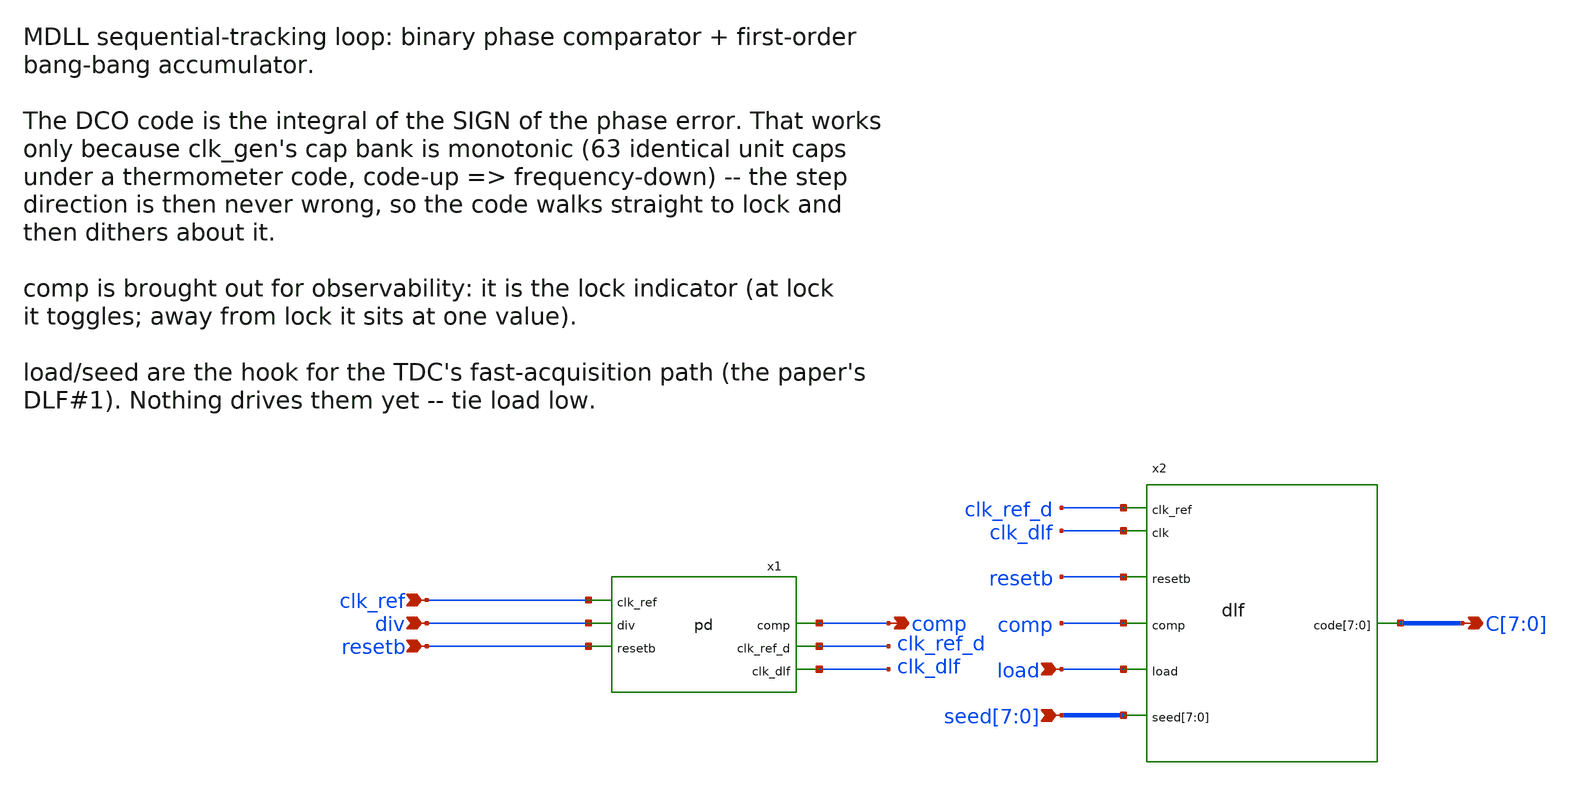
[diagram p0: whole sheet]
** sch_path: TPU5555-main/mdll/mixed_signal_design_blocks/bbpd/src/bbpd.sch
* IHP-GmbH/IHP-Open-PDK/ihp-sg13g2/libs.tech/xschem/sg13g2_stdcells/sg13g2_buf_4.sch:
* Copyright 2023 IHP PDK Authors
* Licensed under the Apache License, Version 2.0 (the "License");
**.subckt bbpd clk_ref div resetb load
*+ seed[7],seed[6],seed[5],seed[4],seed[3],seed[2],seed[1],seed[0] C[7],C[6],C[5],C[4],C[3],C[2],C[1],C[0] comp
*.ipin clk_ref
*.ipin div
*.ipin resetb
*.ipin load
*.ipin seed[7],seed[6],seed[5],seed[4],seed[3],seed[2],seed[1],seed[0]
*.opin C[7],C[6],C[5],C[4],C[3],C[2],C[1],C[0]
*.opin comp
x1 clk_ref div resetb comp clk_ref_d clk_dlf pd
x2 clk_ref_d clk_dlf resetb comp load seed[7] seed[6] seed[5] seed[4] seed[3] seed[2] seed[1]
+ seed[0] C[7] C[6] C[5] C[4] C[3] C[2] C[1] C[0] dlf
**.ends

* expanding   symbol:  bbpd/src/pd.sym # of pins=6
** sym_path: TPU5555-main/mdll/mixed_signal_design_blocks/bbpd/src/pd.sym
** sch_path: TPU5555-main/mdll/mixed_signal_design_blocks/bbpd/src/pd.sch
.subckt pd clk_ref div resetb comp clk_ref_d clk_dlf
*.ipin div
*.ipin clk_ref
*.ipin resetb
*.opin comp
*.opin clk_ref_d
*.opin clk_dlf
x1 comp_raw div clk_ref resetb VDD VSS sg13g2_dfrbpq_1
x2 comp clk_x2 comp_raw resetb VDD VSS sg13g2_dfrbpq_2
x7 clk_x2 clk_ref_d VDD VSS sg13g2_dlygate4sd3_1
x6 clk_ref_d clk_ref VDD VSS sg13g2_buf_2
x8 net1 clk_x2 VDD VSS sg13g2_dlygate4sd3_1
x9 net2 net1 VDD VSS sg13g2_dlygate4sd3_1
x10 clk_dlf net2 VDD VSS sg13g2_buf_4
.ends


* expanding   symbol:  sg13g2_dfrbpq_1.sym # of pins=4
** sym_path: sg13g2_dfrbpq_1.sym
** sch_path: sg13g2_dfrbpq_1.sch
.subckt sg13g2_dfrbpq_1 Q CLK D RESET_B VDD VSS
*.opin Q
*.ipin CLK
*.ipin D
*.ipin RESET_B
*.iopin VDD
*.iopin VSS
XM1 Db D net10 VSS sg13_lv_nmos w=420.00n l=130.00n ng=1 m=1 mm_ok=1
XM2 net10 RESET_B VSS VSS sg13_lv_nmos w=420.00n l=130.00n ng=1 m=1 mm_ok=1
XM3 net1 clkneg net9 VSS sg13_lv_nmos w=420.00n l=130.00n ng=1 m=1 mm_ok=1
XM4 net9 net1 VSS VSS sg13_lv_nmos w=420.00n l=130.00n ng=1 m=1 mm_ok=1
XM5 net1 net1 net5 VSS sg13_lv_nmos w=420.00n l=130.00n ng=1 m=1 mm_ok=1
XM6 net5 RESET_B VSS VSS sg13_lv_nmos w=420.00n l=130.00n ng=1 m=1 mm_ok=1
XM7 net2 net1 VSS VSS sg13_lv_nmos w=740.00n l=130.00n ng=1 m=1 mm_ok=1
XM8 Q net2 VSS VSS sg13_lv_nmos w=740.00n l=130.00n ng=1 m=1 mm_ok=1
XM9 clkneg CLK VSS VSS sg13_lv_nmos w=740.00n l=130.00n ng=1 m=1 mm_ok=1
XM10 clkpos clkneg VSS VSS sg13_lv_nmos w=740.00n l=130.00n ng=1 m=1 mm_ok=1
XM11 Db clkneg net3 VSS sg13_lv_nmos w=420.00n l=130.00n ng=1 m=1 mm_ok=1
XM12 net3 clkpos net8 VSS sg13_lv_nmos w=420.00n l=130.00n ng=1 m=1 mm_ok=1
XM13 net8 net3 net4 VSS sg13_lv_nmos w=420.00n l=130.00n ng=1 m=1 mm_ok=1
XM14 net4 RESET_B VSS VSS sg13_lv_nmos w=420.00n l=130.00n ng=1 m=1 mm_ok=1
XM15 net3 net3 VSS VSS sg13_lv_nmos w=740.00n l=130.00n ng=1 m=1 mm_ok=1
XM16 net3 clkpos net1 VSS sg13_lv_nmos w=740.00n l=130.00n ng=1 m=1 mm_ok=1
XM17 Db RESET_B VDD VDD sg13_lv_pmos w=420.00n l=130.00n ng=1 m=1 mm_ok=1
XM18 Db D VDD VDD sg13_lv_pmos w=420.00n l=130.00n ng=1 m=1 mm_ok=1
XM19 net7 net1 VDD VDD sg13_lv_pmos w=420.00n l=130.00n ng=1 m=1 mm_ok=1
XM20 net1 clkpos net7 VDD sg13_lv_pmos w=420.00n l=130.00n ng=1 m=1 mm_ok=1
XM21 net1 net1 VDD VDD sg13_lv_pmos w=420.00n l=130.00n ng=1 m=1 mm_ok=1
XM22 net1 RESET_B VDD VDD sg13_lv_pmos w=420.00n l=130.00n ng=1 m=1 mm_ok=1
XM23 net2 net1 VDD VDD sg13_lv_pmos w=1.12u l=130.00n ng=1 m=1 mm_ok=1
XM24 Q net2 VDD VDD sg13_lv_pmos w=1.12u l=130.00n ng=1 m=1 mm_ok=1
XM25 clkneg CLK VDD VDD sg13_lv_pmos w=1.12u l=130.00n ng=1 m=1 mm_ok=1
XM26 clkpos clkneg VDD VDD sg13_lv_pmos w=1.12u l=130.00n ng=1 m=1 mm_ok=1
XM27 Db clkpos net3 VDD sg13_lv_pmos w=420.00n l=130.00n ng=1 m=1 mm_ok=1
XM28 net6 net3 VDD VDD sg13_lv_pmos w=420.00n l=130.00n ng=1 m=1 mm_ok=1
XM29 net3 clkneg net6 VDD sg13_lv_pmos w=420.00n l=130.00n ng=1 m=1 mm_ok=1
XM30 net3 RESET_B VDD VDD sg13_lv_pmos w=420.00n l=130.00n ng=1 m=1 mm_ok=1
XM31 net3 net3 VDD VDD sg13_lv_pmos w=1.000u l=130.00n ng=1 m=1 mm_ok=1
XM32 net3 clkneg net1 VDD sg13_lv_pmos w=1.000u l=130.00n ng=1 m=1 mm_ok=1
.ends


* expanding   symbol:  sg13g2_dfrbpq_2.sym # of pins=4
** sym_path: sg13g2_dfrbpq_2.sym
** sch_path: sg13g2_dfrbpq_2.sch
.subckt sg13g2_dfrbpq_2 Q CLK D RESET_B VDD VSS
*.opin Q
*.ipin CLK
*.ipin D
*.ipin RESET_B
*.iopin VDD
*.iopin VSS
XM1 Db D net12 VSS sg13_lv_nmos w=420.00n l=130.00n ng=1 m=1 mm_ok=1
XM2 net12 RESET_B VSS VSS sg13_lv_nmos w=420.00n l=130.00n ng=1 m=1 mm_ok=1
XM3 net2 clkneg net11 VSS sg13_lv_nmos w=420.00n l=130.00n ng=1 m=1 mm_ok=1
XM4 net11 net3 VSS VSS sg13_lv_nmos w=420.00n l=130.00n ng=1 m=1 mm_ok=1
XM5 net3 net2 net7 VSS sg13_lv_nmos w=420.00n l=130.00n ng=1 m=1 mm_ok=1
XM6 net7 RESET_B VSS VSS sg13_lv_nmos w=420.00n l=130.00n ng=1 m=1 mm_ok=1
XM7 net1 net2 VSS VSS sg13_lv_nmos w=640.00n l=130.00n ng=1 m=1 mm_ok=1
XM8 Q net1 VSS VSS sg13_lv_nmos w=1.48u l=130.00n ng=2 m=1 mm_ok=1
XM9 clkneg CLK VSS VSS sg13_lv_nmos w=740.00n l=130.00n ng=1 m=1 mm_ok=1
XM10 clkpos clkneg VSS VSS sg13_lv_nmos w=740.00n l=130.00n ng=1 m=1 mm_ok=1
XM11 Db clkneg net4 VSS sg13_lv_nmos w=420.00n l=130.00n ng=1 m=1 mm_ok=1
XM12 net4 clkpos net10 VSS sg13_lv_nmos w=420.00n l=130.00n ng=1 m=1 mm_ok=1
XM13 net10 net5 net6 VSS sg13_lv_nmos w=420.00n l=130.00n ng=1 m=1 mm_ok=1
XM14 net6 RESET_B VSS VSS sg13_lv_nmos w=420.00n l=130.00n ng=1 m=1 mm_ok=1
XM15 net5 net4 VSS VSS sg13_lv_nmos w=740.00n l=130.00n ng=1 m=1 mm_ok=1
XM16 net5 clkpos net2 VSS sg13_lv_nmos w=740.00n l=130.00n ng=1 m=1 mm_ok=1
XM17 Db RESET_B VDD VDD sg13_lv_pmos w=420.00n l=130.00n ng=1 m=1 mm_ok=1
XM18 Db D VDD VDD sg13_lv_pmos w=420.00n l=130.00n ng=1 m=1 mm_ok=1
XM19 net9 net3 VDD VDD sg13_lv_pmos w=420.00n l=130.00n ng=1 m=1 mm_ok=1
XM20 net2 clkpos net9 VDD sg13_lv_pmos w=420.00n l=130.00n ng=1 m=1 mm_ok=1
XM21 net3 net2 VDD VDD sg13_lv_pmos w=420.00n l=130.00n ng=1 m=1 mm_ok=1
XM22 net3 RESET_B VDD VDD sg13_lv_pmos w=420.00n l=130.00n ng=1 m=1 mm_ok=1
XM23 net1 net2 VDD VDD sg13_lv_pmos w=1.000u l=130.00n ng=1 m=1 mm_ok=1
XM24 Q net1 VDD VDD sg13_lv_pmos w=2.24u l=130.00n ng=2 m=1 mm_ok=1
XM25 clkneg CLK VDD VDD sg13_lv_pmos w=1.12u l=130.00n ng=1 m=1 mm_ok=1
XM26 clkpos clkneg VDD VDD sg13_lv_pmos w=1.12u l=130.00n ng=1 m=1 mm_ok=1
XM27 Db clkpos net4 VDD sg13_lv_pmos w=420.00n l=130.00n ng=1 m=1 mm_ok=1
XM28 net8 net5 VDD VDD sg13_lv_pmos w=420.00n l=130.00n ng=1 m=1 mm_ok=1
XM29 net4 clkneg net8 VDD sg13_lv_pmos w=420.00n l=130.00n ng=1 m=1 mm_ok=1
XM30 net4 RESET_B VDD VDD sg13_lv_pmos w=420.00n l=130.00n ng=1 m=1 mm_ok=1
XM31 net5 net4 VDD VDD sg13_lv_pmos w=1.000u l=130.00n ng=1 m=1 mm_ok=1
XM32 net5 clkneg net2 VDD sg13_lv_pmos w=1.000u l=130.00n ng=1 m=1 mm_ok=1
.ends


* expanding   symbol:  sg13g2_dlygate4sd3_1.sym # of pins=2
** sym_path: sg13g2_dlygate4sd3_1.sym
** sch_path: sg13g2_dlygate4sd3_1.sch
.subckt sg13g2_dlygate4sd3_1 X A VDD VSS
*.ipin A
*.opin X
*.iopin VDD
*.iopin VSS
XM1 net3 A VSS VSS sg13_lv_nmos w=420.00n l=130.00n ng=1 m=1 mm_ok=1
XM2 net1 net3 VSS VSS sg13_lv_nmos w=420.00n l=500.0n ng=1 m=1 mm_ok=1
XM3 net2 net1 VSS VSS sg13_lv_nmos w=420.00n l=500.0n ng=1 m=1 mm_ok=1
XM4 X net2 VSS VSS sg13_lv_nmos w=740.00n l=130.00n ng=1 m=1 mm_ok=1
XM5 net3 A VDD VDD sg13_lv_pmos w=420.00n l=130.00n ng=1 m=1 mm_ok=1
XM6 net1 net3 VDD VDD sg13_lv_pmos w=1.000u l=500.0n ng=1 m=1 mm_ok=1
XM7 net2 net1 VDD VDD sg13_lv_pmos w=1.000u l=500.0n ng=1 m=1 mm_ok=1
XM8 X net2 VDD VDD sg13_lv_pmos w=1.12u l=130.00n ng=1 m=1 mm_ok=1
.ends


* expanding   symbol:  sg13g2_buf_2.sym # of pins=2
** sym_path: sg13g2_buf_2.sym
** sch_path: sg13g2_buf_2.sch
.subckt sg13g2_buf_2 X A VDD VSS
*.ipin A
*.opin X
*.iopin VDD
*.iopin VSS
XM1 net1 A VSS VSS sg13_lv_nmos w=640.00n l=130.00n ng=1 m=1 mm_ok=1
XM2 X net1 VSS VSS sg13_lv_nmos w=1.48u l=130.00n ng=2 m=1 mm_ok=1
XM3 net1 A VDD VDD sg13_lv_pmos w=1.000u l=130.00n ng=1 m=1 mm_ok=1
XM4 X net1 VDD VDD sg13_lv_pmos w=2.24u l=130.00n ng=2 m=1 mm_ok=1
.ends


* expanding   symbol:  sg13g2_buf_4.sym # of pins=2
** sym_path: sg13g2_buf_4.sym
** sch_path: sg13g2_buf_4.sch
.subckt sg13g2_buf_4 X A VDD VSS
*.ipin A
*.opin X
*.iopin VDD
*.iopin VSS
XM1 net1 A VSS VSS sg13_lv_nmos w=740.00n l=130.00n ng=1 m=1 mm_ok=1
XM2 X net1 VSS VSS sg13_lv_nmos w=2.96u l=130.00n ng=4 m=1 mm_ok=1
XM3 net1 A VDD VDD sg13_lv_pmos w=1.68u l=130.00n ng=2 m=1 mm_ok=1
XM4 X net1 VDD VDD sg13_lv_pmos w=4.48u l=130.00n ng=4 m=1 mm_ok=1
.ends

.end
